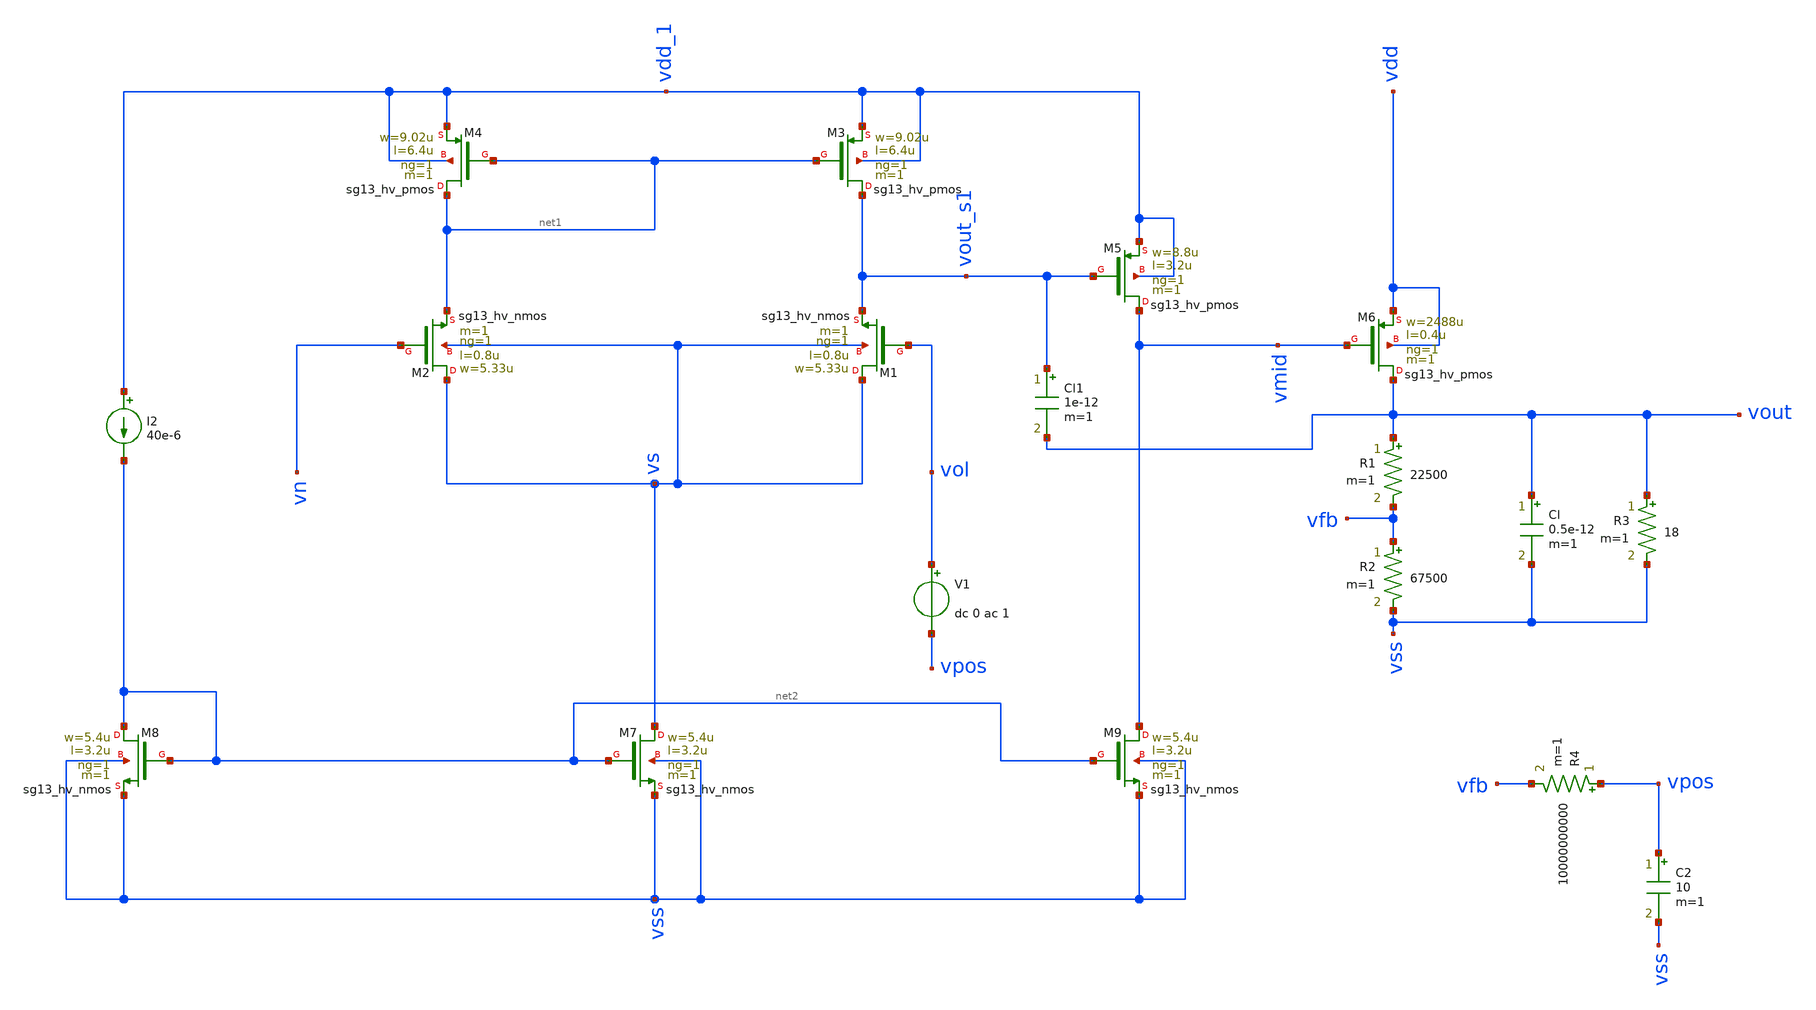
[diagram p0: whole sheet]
** sch_path: test/Tesis_notebooks/xschem/ldo_ol_tb.sch
**.subckt ldo_ol_tb
R1 vout vfb 22500 m=1
R2 vfb vss 67500 m=1
Cl vout vss 0.5e-12 m=1
XM1 vs vol vout_s1 vs sg13_hv_nmos w=5.33u l=0.8u ng=1 m=1 mm_ok=1
XM2 vs vn net1 vs sg13_hv_nmos w=5.33u l=0.8u ng=1 m=1 mm_ok=1
XM3 vout_s1 net1 vdd_1 vdd_1 sg13_hv_pmos w=9.02u l=6.4u ng=1 m=1 mm_ok=1
XM4 net1 net1 vdd_1 vdd_1 sg13_hv_pmos w=9.02u l=6.4u ng=1 m=1 mm_ok=1
XM5 vmid vout_s1 vdd_1 vdd_1 sg13_hv_pmos w=8.8u l=3.2u ng=1 m=1 mm_ok=1
XM6 vout vmid vdd vdd sg13_hv_pmos w=2488u l=0.4u ng=1 m=1 mm_ok=1
R4 vpos vfb 10000000000 m=1
C2 vpos vss 10 m=1
V1 vol vpos dc 0 ac 1
R3 vout vss 18 m=1
XM7 vs net2 vss vss sg13_hv_nmos w=5.4u l=3.2u ng=1 m=1 mm_ok=1
XM8 net2 net2 vss vss sg13_hv_nmos w=5.4u l=3.2u ng=1 m=1 mm_ok=1
XM9 vmid net2 vss vss sg13_hv_nmos w=5.4u l=3.2u ng=1 m=1 mm_ok=1
I2 vdd_1 net2 40e-6
Cl1 vout_s1 vout 1e-12 m=1
**** begin user architecture code



.lib /opt/pdks/ihp-sg13g2/libs.tech/ngspice/models/cornerMOShv.lib mos_tt

Vref vn 0 1.35
Vdd vdd 0 3.3
Vdd_1 vdd_1 0 3.3
Vss vss 0 0

.control
ac dec 10 1 10G
plot vdb(vout)
plot phase(vout)*180/PI
op
print vout vmid vout_s1 vs

let gm_m1 = @n.xm1.nsg13_hv_nmos[gm]
let gm_m2 = @n.xm2.nsg13_hv_nmos[gm]
let gm_m3 = @n.xm3.nsg13_hv_pmos[gm]
let gm_m4 = @n.xm4.nsg13_hv_pmos[gm]
let gm_m5 = @n.xm5.nsg13_hv_pmos[gm]
let gm_m6 = @n.xm6.nsg13_hv_pmos[gm]

let gds_m1 = @n.xm1.nsg13_hv_nmos[gds]
let gds_m2 = @n.xm2.nsg13_hv_nmos[gds]
let gds_m3 = @n.xm3.nsg13_hv_pmos[gds]
let gds_m4 = @n.xm4.nsg13_hv_pmos[gds]
let gds_m5 = @n.xm5.nsg13_hv_pmos[gds]
let gds_m6 = @n.xm6.nsg13_hv_pmos[gds]

print gm_m1
print gm_m2
print gm_m3
print gm_m4
print gm_m5
print gm_m6

print 1/gds_m1
print 1/gds_m2
print 1/gds_m3
print 1/gds_m4
print 1/gds_m5
print 1/gds_m6

.endc



**** end user architecture code
**.ends
.end
